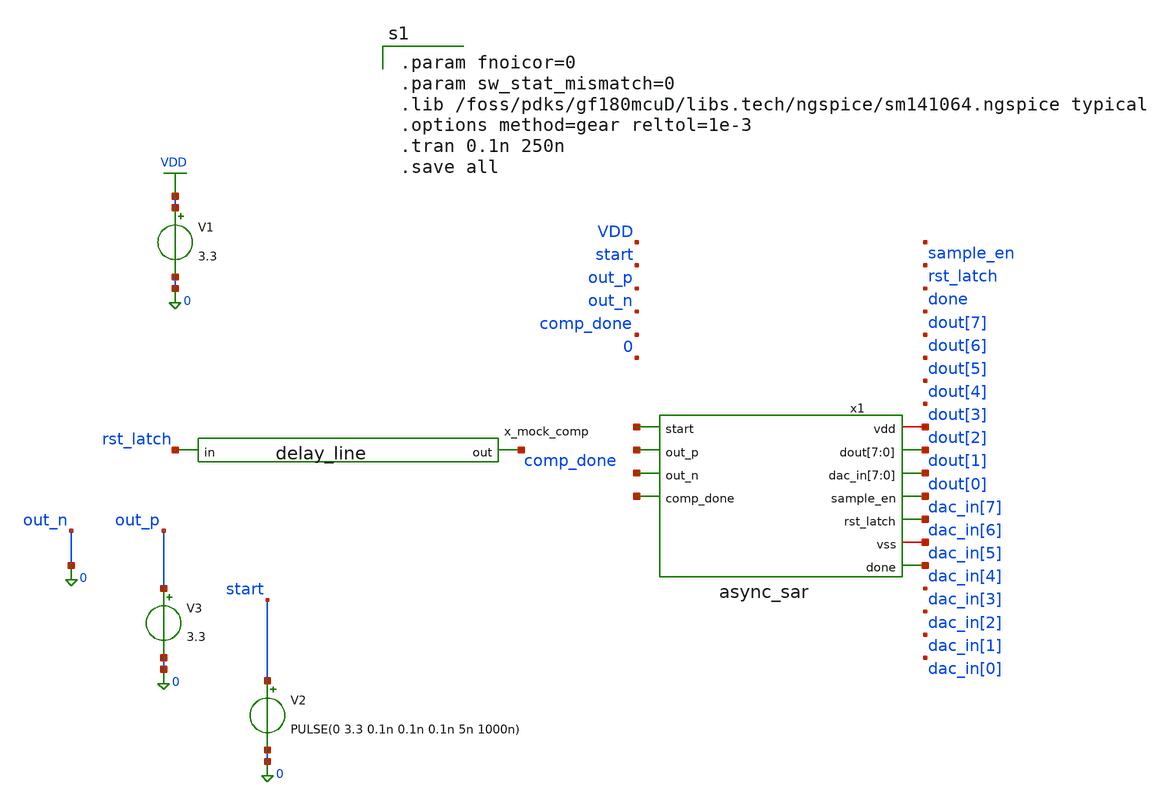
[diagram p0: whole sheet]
** sch_path: xschem/sar_adc/tb_async_sar.sch
**.subckt tb_async_sar
V1 VDD 0 3.3
V2 start 0 PULSE(0 3.3 0.1n 0.1n 0.1n 5n 1000n)
V3 out_p 0 3.3
x_mock_comp comp_done rst_latch delay_line
x1 dout[2] net1 dout[1] dout[1] dout[1] dout[1] dout[1] dout[1] dout[1] dout[1] net2 dout[0] dout[0]
+ dout[0] dout[0] dout[0] dout[0] dout[0] dout[0] net3 dac_in[7] dac_in[6] net4 dac_in[5] dac_in[4] async_sar
**** begin user architecture code

.param fnoicor=0
.param sw_stat_mismatch=0
.lib /foss/pdks/gf180mcuD/libs.tech/ngspice/sm141064.ngspice typical
.options method=gear reltol=1e-3
.tran 0.1n 250n
.save all

**** end user architecture code
**.ends
.GLOBAL VDD
.end
